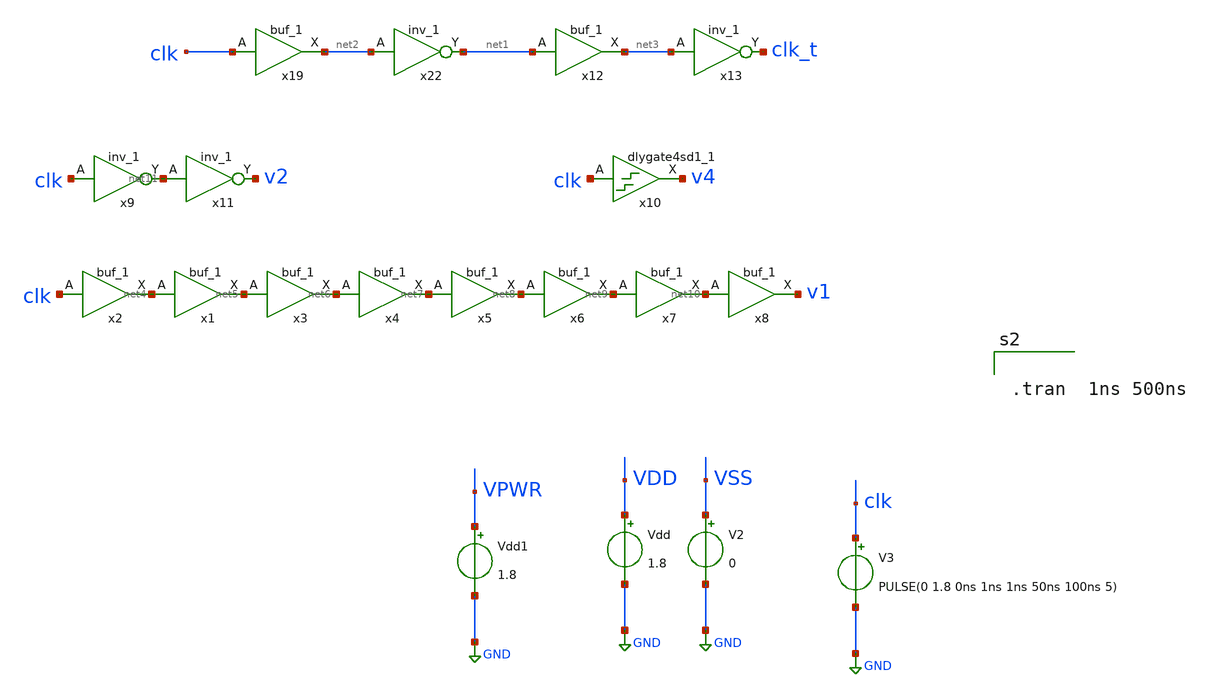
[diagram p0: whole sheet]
** sch_path: buffer_tb.sch
**.subckt buffer_tb
x2 clk VGND VNB VPB VPWR net4 sky130_fd_sc_hd__buf_1
x1 net4 VGND VNB VPB VPWR net5 sky130_fd_sc_hd__buf_1
x3 net5 VGND VNB VPB VPWR net6 sky130_fd_sc_hd__buf_1
x4 net6 VGND VNB VPB VPWR net7 sky130_fd_sc_hd__buf_1
x5 net7 VGND VNB VPB VPWR net8 sky130_fd_sc_hd__buf_1
x6 net8 VGND VNB VPB VPWR net9 sky130_fd_sc_hd__buf_1
x7 net9 VGND VNB VPB VPWR net10 sky130_fd_sc_hd__buf_1
x8 net10 VGND VNB VPB VPWR v1 sky130_fd_sc_hd__buf_1
x10 clk VGND VNB VPB VPWR v4 sky130_fd_sc_hd__dlygate4sd1_1
x11 net11 VGND VNB VPB VPWR v2 sky130_fd_sc_hd__inv_1
x9 clk VGND VNB VPB VPWR net11 sky130_fd_sc_hd__inv_1
x19 clk VSS VNB VPB VDD net2 sky130_fd_sc_hd__buf_1
x22 net2 VSS VNB VPB VDD net1 sky130_fd_sc_hd__inv_1
V3 clk GND PULSE(0 1.8 0ns 1ns 1ns 50ns 100ns 5)
x12 net1 VSS VNB VPB VDD net3 sky130_fd_sc_hd__buf_1
x13 net3 VSS VNB VPB VDD clk_t sky130_fd_sc_hd__inv_1
Vdd VDD GND 1.8
V2 VSS GND 0
Vdd1 VPWR GND 1.8
**** begin user architecture code

** opencircuitdesign pdks install
.lib $::SKYWATER_MODELS/sky130.lib.spice tt
.include $::SKYWATER_STDCELLS/sky130_fd_sc_hd.spice




.tran  1ns 500ns




**** end user architecture code
**.ends
.GLOBAL GND
.end
